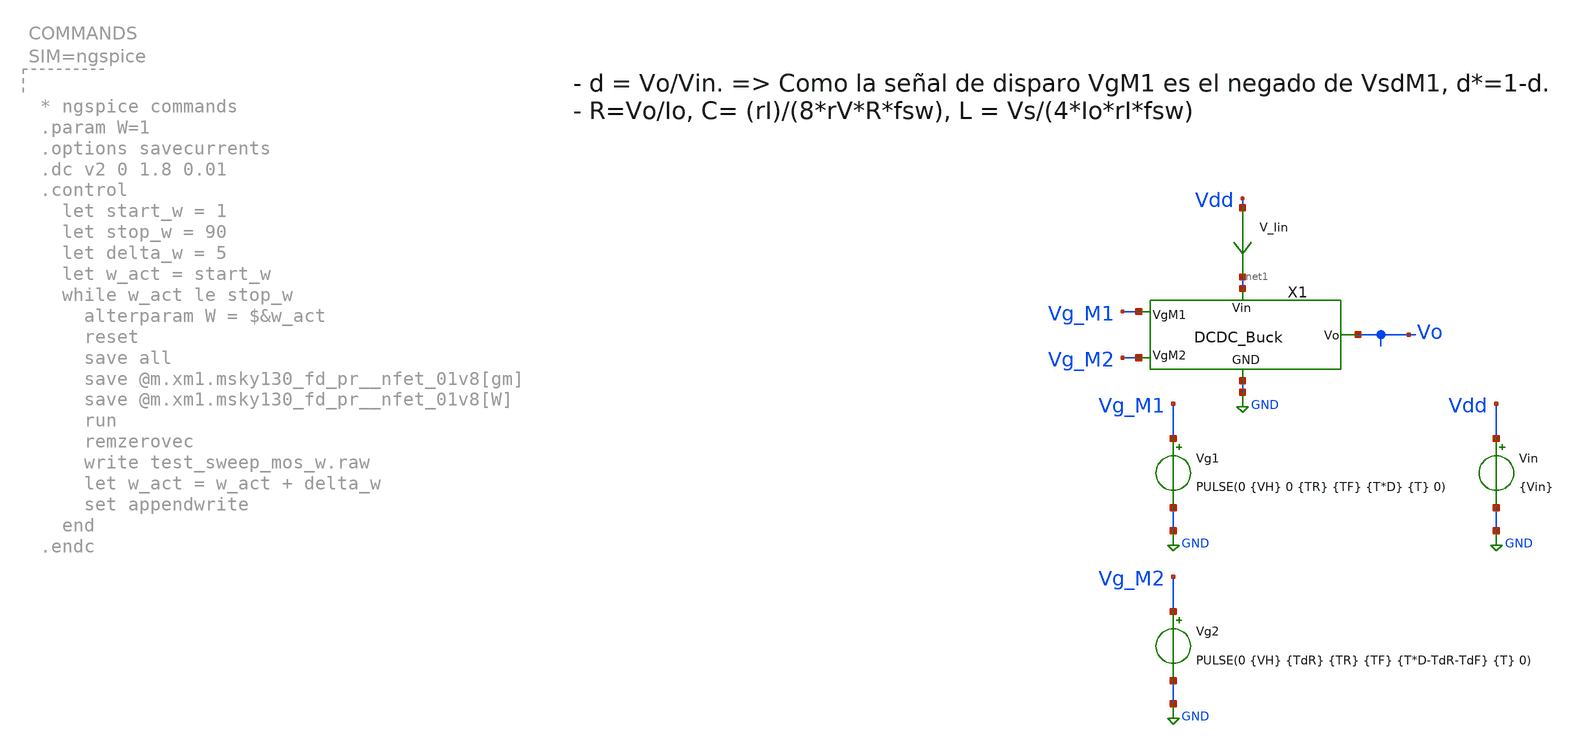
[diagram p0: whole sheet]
** sch_path: xschem/DCDCBuck/TB_DCDCBuck_Sweep.sch
**.subckt TB_DCDCBuck_Sweep
Vin Vdd GND {Vin}
Vg2 Vg_M2 GND PULSE(0 {VH} {TdR} {TR} {TF} {T*D-TdR-TdF} {T} 0)
Vg1 Vg_M1 GND PULSE(0 {VH} 0 {TR} {TF} {T*D} {T} 0)
V_Iin Vdd net1 0
.save i(v_iin)
X1 Vg_M1 Vg_M2 GND net1 Vo DCDC_Buck
**** begin user architecture code


.param Vin = 1.8
.param VH = 1.8
.param Del = 0

.ic v(Vo) = 0
*.ic i(x1.L1) = 0 No se puede hacer ic de corriente
*.ic v(Vc) = 0

.param fsw = 20Meg
*.param fsw = 10Meg
*.param fsw = 8.4Meg
*.param fsw = 1Meg

.param Vo = 1.2
.param Io = 1
.param rI = 0.3
.param rV = 0.1
.param T = 1/fsw

.param D = 1-((Vo+0.05)/(Vin-0.03))
.param TR = 1n
.param TF = 1n
.param TdR = 0.5n
.param TdF = 0.5n

*Filtro
.param L = Vin/(4*Io*rI*fsw)
.param R = Vo/Io
.param C = rI/(8*rV*R*fsw)

*.option temp = 125
*.option temp = -40
.option temp = 27




.lib /opt/pdks/sky130A/libs.tech/ngspice/sky130.lib.spice tt
*.lib /opt/pdks/sky130A/libs.tech/ngspice/sky130.lib.spice ss
*.lib /opt/pdks/sky130A/libs.tech/ngspice/sky130.lib.spice ff
*.lib /opt/pdks/sky130A/libs.tech/ngspice/sky130.lib.spice sf
*.lib /opt/pdks/sky130A/libs.tech/ngspice/sky130.lib.spice fs



.param temp=27
.param mult_M1 = 9000
.param w_M1 =10
.param l_M1 = 0.15
.param ng_M1 = 1

.param mult_M2 = 2000
.param w_M2 =10
.param l_M2 =0.15
.param ng_M2 =1







.save all
.param tau = 4*L/R
.csparam tau = {tau}
.param SimTime = tau+10*T
.csparam Sim_end = {SimTime}
.csparam Vo = {Vo}
.csparam T = {T}
.csparam L = {L}
.csparam C = {C}
.csparam R = {R}
.csparam fsw = {fsw}

.param start = 0.6
.param stop = 2.4
.param step = 0.2

.tran 10n {SimTime} uic

.control
set color0 = white

let strt = 1
let stp = 21
let step = 4

compose fsw_sweep start = 1Meg stop = 21Meg step = 4Meg
*compose Io_sweep2 start = 0.5 stop = 2 step=0.1
*compose R_sweep start=0.6 stop=2.4 step=0.2

*let R_sweep = {Vo}/Io_sweep2
let T_sweep = 1/fsw_sweep
let len = 1+(stp-strt)/step

let eff_sweep = vector(len)
*let fsw_sweep = vector(len)
let Io_sweep = vector(len)
let Vo_sweep = vector(len)
let Po_sweep = vector(len)
let Pin_sweep = vector(len)
let loss_M1_sweep = vector(len)
let loss_M2_sweep = vector(len)

let index = 0

foreach T_val $&T_sweep
	alterparam fsw = $fsw_val
	alterparam T = $T_val
	reset
	save all
	run
	let Io = i(v.x1.V_Io)
	*let Id_M1 = @m.x1.xm1.msky130_fd_pr__pfet_01v8[id]
	let Id_M1 = i(V_Iin)
	*let Id_M2 = @m.x1.xm2.msky130_fd_pr__nfet_01v8[id]
	let Id_M2 = -i(v.x1.V_IM2)
	let gds_M1 = @m.x1.xm1.msky130_fd_pr__pfet_01v8[gds]
	let gds_M2 = @m.x1.xm2.msky130_fd_pr__nfet_01v8[gds]

	let Po = Io*v(Vo)
	let I_in = i(V_Iin)
	let Pin = I_in*v(Vdd)
	let Vsd_M1 = v(Vdd) - v(x1.Vc)
	let Vds_M2 = v(x1.Vc)
	let P_M1 = Vsd_M1*Id_M1
	let P_M2 = -Vds_M2*Id_M2
	let Ron_M1 = Vsd_M1/Id_M1
	let Ron_M2 = Vds_M2/Id_M2
	*let Ron_M1 = 1/gds_M1
	*let Ron_M2 = 1/gds_M2

	let Tmeas_i = {Sim_end} - 5*{T}
	let Tmeas_end = {Sim_end}

	*plot v(Vo)
	*plot Io i(v.x1.V_IL)
	*plot Id_M1 Id_M2
	*plot Po Pin
	*plot P_M1 P_M2
	*plot v(x1.Vc)
	*plot v(Vg_M1) v(Vg_M2)
	*plot Ron_M1 Ron_M2

	meas tran Vo_mean AVG v(Vo) FROM={Tmeas_i} TO={Tmeas_end}
	meas tran Io_mean AVG Io FROM={Tmeas_i} TO={Tmeas_end}
	meas tran Irms_M1 RMS Id_M1 FROM={Tmeas_i} TO={Tmeas_end}
	meas tran Irms_M2 RMS Id_M2 FROM={Tmeas_i} TO={Tmeas_end}
	meas tran Po_mean AVG Po FROM={Tmeas_i} TO={Tmeas_end}
	meas tran Pin_mean AVG Pin FROM={Tmeas_i} TO={Tmeas_end}
	meas tran P_M1_mean AVG P_M1 FROM={Tmeas_i} TO={Tmeas_end}
	meas tran P_M2_mean AVG P_M2 FROM={Tmeas_i} TO={Tmeas_end}

	let eff = 100*Po_mean/Pin_mean
	let loss_M1 = 100*P_M1_mean/Pin_mean
	let loss_M2 = 100*P_M2_mean/Pin_mean
	let cond_loss_M1 = Irms_M1*Irms_M1*40m*100
	let cond_loss_M2 = Irms_M2*Irms_M2*35m*100
	let sumaPot = eff+loss_M1+loss_M2
	print eff loss_M1 loss_M2 cond_loss_M1 cond_loss_M2 sumaPot
	print tau T L C R

	let eff_sweep[index] =  eff
	let Io_sweep[index] = Io_mean
	let Vo_sweep[index] = Vo_mean
	let Po_sweep[index] = Po_mean
	let Pin_sweep[index] = Pin_mean

	let loss_M1_sweep[index] = loss_M1
	let loss_M2_sweep[index] = loss_M2

	let index = index + 1

	*write TB_DCDCBuck.raw
end
*print eff loss_M1_sweep loss_M2_sweep
print eff_sweep loss_M2_sweep loss_M1_sweep
print fsw_sweep Io_sweep Vo_sweep
print Po_sweep Pin_sweep
plot eff_sweep vs fsw_sweep
plot Io_sweep vs fsw_sweep
plot Vo_sweep vs fsw_sweep
plot Pin_sweep Po_sweep vs fsw_sweep
plot loss_M1_sweep loss_M2_sweep vs fsw_sweep
.endc


.end





**** end user architecture code
**.ends

* expanding   symbol:  ../DCDCBuck/DCDC_Buck.sym # of pins=5
** sym_path: xschem/DCDCBuck/DCDC_Buck.sym
** sch_path: xschem/DCDCBuck/DCDC_Buck.sch
.subckt DCDC_Buck VgM1 VgM2 GND Vin Vo
*.iopin Vin
*.ipin VgM1
*.ipin VgM2
*.iopin Vo
*.iopin GND
L1 net2 net1 {L} m=1
C1 net1 GND {C} m=1
V_Io net1 Vo 0
.save i(v_io)
V_IL Vc net2 0
.save i(v_il)
R1 Vo GND {R} m=1
V_IM2 Vc net3 0
.save i(v_im2)
XM3 Vc VgM1 Vin Vin sg13_hv_pmos w={w_M1} l={l_M1} ng={ng_M1} m={mult_M1} mm_ok=1
XM1 GND VgM2 net3 GND sg13_hv_nmos w={w_M2} l={l_M2} ng={ng_M2} m={mult_M2} mm_ok=1
.ends

.GLOBAL GND
.end
